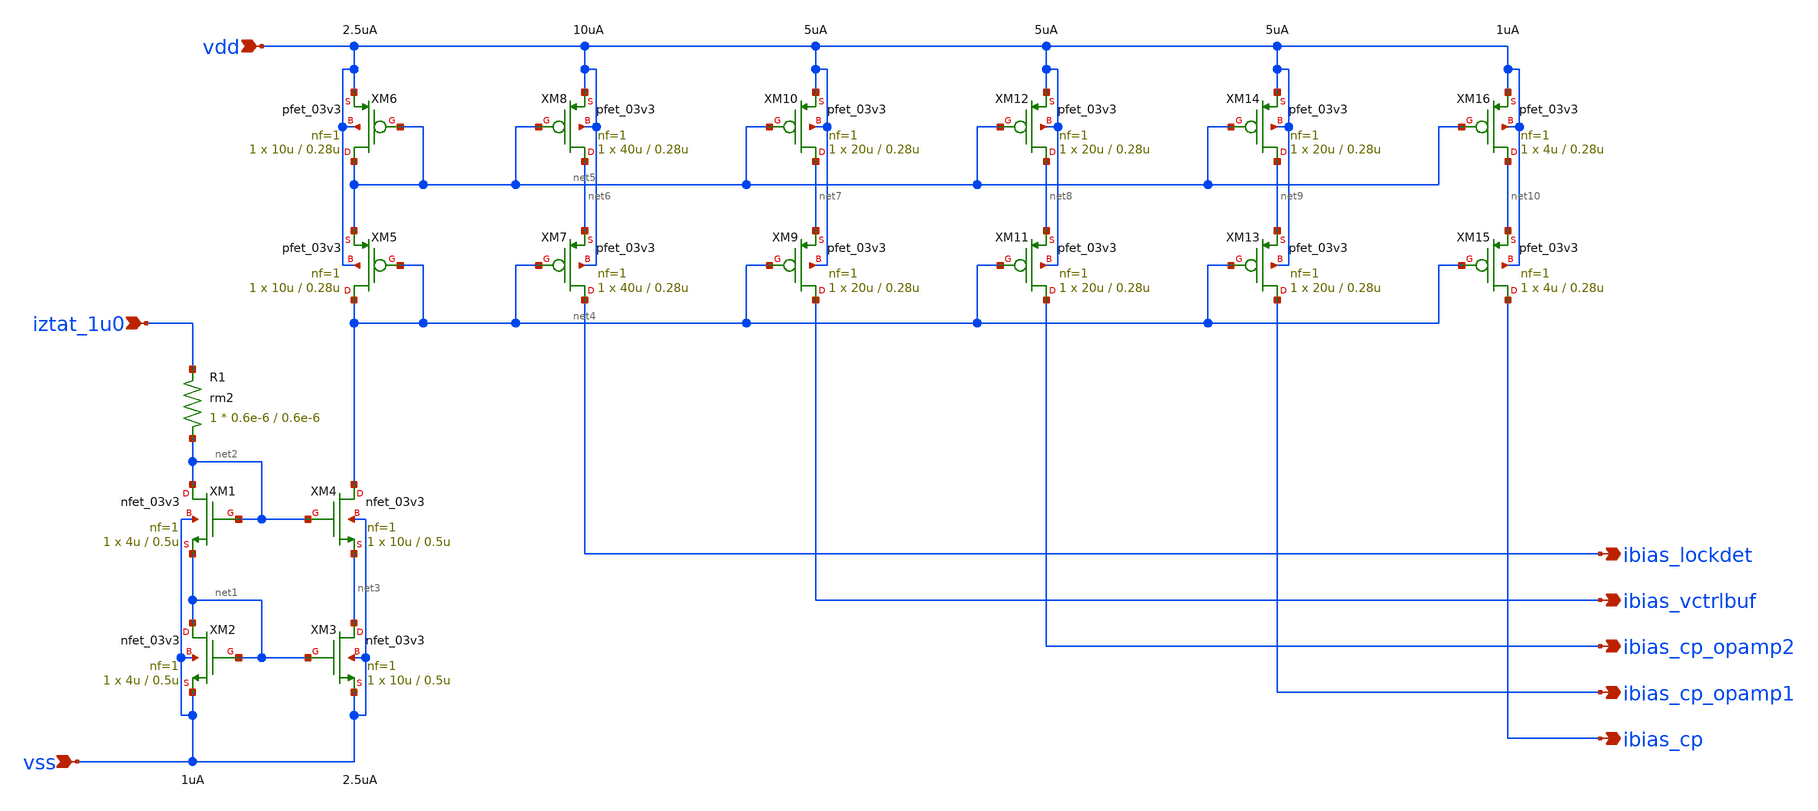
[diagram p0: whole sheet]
** sch_path: xschem/pll_ibias_generator.sch
**.subckt pll_ibias_generator iztat_1u0 vss vdd ibias_cp ibias_cp_opamp1 ibias_cp_opamp2
*+ ibias_vctrlbuf ibias_lockdet
*.ipin iztat_1u0
*.ipin vss
*.ipin vdd
*.opin ibias_cp
*.opin ibias_cp_opamp1
*.opin ibias_cp_opamp2
*.opin ibias_vctrlbuf
*.opin ibias_lockdet
XM2 net1 net1 vss vss nfet_03v3 L=0.5u W=4u nf=1 ad='int((nf+1)/2) * W/nf * 0.18u' as='int((nf+2)/2) * W/nf * 0.18u'
+ pd='2*int((nf+1)/2) * (W/nf + 0.18u)' ps='2*int((nf+2)/2) * (W/nf + 0.18u)' nrd='0.18u / W' nrs='0.18u / W'
+ sa=0 sb=0 sd=0 m=1
XM1 net2 net2 net1 vss nfet_03v3 L=0.5u W=4u nf=1 ad='int((nf+1)/2) * W/nf * 0.18u' as='int((nf+2)/2) * W/nf * 0.18u'
+ pd='2*int((nf+1)/2) * (W/nf + 0.18u)' ps='2*int((nf+2)/2) * (W/nf + 0.18u)' nrd='0.18u / W' nrs='0.18u / W'
+ sa=0 sb=0 sd=0 m=1
XR1 net2 iztat_1u0 rm2 r_width=0.6e-6 r_length=0.6e-6 m=1
XM3 net3 net1 vss vss nfet_03v3 L=0.5u W=10u nf=1 ad='int((nf+1)/2) * W/nf * 0.18u' as='int((nf+2)/2) * W/nf * 0.18u'
+ pd='2*int((nf+1)/2) * (W/nf + 0.18u)' ps='2*int((nf+2)/2) * (W/nf + 0.18u)' nrd='0.18u / W' nrs='0.18u / W'
+ sa=0 sb=0 sd=0 m=1
XM4 net4 net2 net3 vss nfet_03v3 L=0.5u W=10u nf=1 ad='int((nf+1)/2) * W/nf * 0.18u' as='int((nf+2)/2) * W/nf * 0.18u'
+ pd='2*int((nf+1)/2) * (W/nf + 0.18u)' ps='2*int((nf+2)/2) * (W/nf + 0.18u)' nrd='0.18u / W' nrs='0.18u / W'
+ sa=0 sb=0 sd=0 m=1
XM5 net4 net4 net5 vdd pfet_03v3 L=0.28u W=10u nf=1 ad='int((nf+1)/2) * W/nf * 0.18u' as='int((nf+2)/2) * W/nf * 0.18u'
+ pd='2*int((nf+1)/2) * (W/nf + 0.18u)' ps='2*int((nf+2)/2) * (W/nf + 0.18u)' nrd='0.18u / W' nrs='0.18u / W'
+ sa=0 sb=0 sd=0 m=1
XM6 net5 net5 vdd vdd pfet_03v3 L=0.28u W=10u nf=1 ad='int((nf+1)/2) * W/nf * 0.18u' as='int((nf+2)/2) * W/nf * 0.18u'
+ pd='2*int((nf+1)/2) * (W/nf + 0.18u)' ps='2*int((nf+2)/2) * (W/nf + 0.18u)' nrd='0.18u / W' nrs='0.18u / W'
+ sa=0 sb=0 sd=0 m=1
XM7 ibias_lockdet net4 net6 vdd pfet_03v3 L=0.28u W=40u nf=1 ad='int((nf+1)/2) * W/nf * 0.18u' as='int((nf+2)/2) * W/nf * 0.18u'
+ pd='2*int((nf+1)/2) * (W/nf + 0.18u)' ps='2*int((nf+2)/2) * (W/nf + 0.18u)' nrd='0.18u / W' nrs='0.18u / W'
+ sa=0 sb=0 sd=0 m=1
XM8 net6 net5 vdd vdd pfet_03v3 L=0.28u W=40u nf=1 ad='int((nf+1)/2) * W/nf * 0.18u' as='int((nf+2)/2) * W/nf * 0.18u'
+ pd='2*int((nf+1)/2) * (W/nf + 0.18u)' ps='2*int((nf+2)/2) * (W/nf + 0.18u)' nrd='0.18u / W' nrs='0.18u / W'
+ sa=0 sb=0 sd=0 m=1
XM9 ibias_vctrlbuf net4 net7 vdd pfet_03v3 L=0.28u W=20u nf=1 ad='int((nf+1)/2) * W/nf * 0.18u' as='int((nf+2)/2) * W/nf * 0.18u'
+ pd='2*int((nf+1)/2) * (W/nf + 0.18u)' ps='2*int((nf+2)/2) * (W/nf + 0.18u)' nrd='0.18u / W' nrs='0.18u / W'
+ sa=0 sb=0 sd=0 m=1
XM10 net7 net5 vdd vdd pfet_03v3 L=0.28u W=20u nf=1 ad='int((nf+1)/2) * W/nf * 0.18u' as='int((nf+2)/2) * W/nf * 0.18u'
+ pd='2*int((nf+1)/2) * (W/nf + 0.18u)' ps='2*int((nf+2)/2) * (W/nf + 0.18u)' nrd='0.18u / W' nrs='0.18u / W'
+ sa=0 sb=0 sd=0 m=1
XM11 ibias_cp_opamp2 net4 net8 vdd pfet_03v3 L=0.28u W=20u nf=1 ad='int((nf+1)/2) * W/nf * 0.18u' as='int((nf+2)/2) * W/nf * 0.18u'
+ pd='2*int((nf+1)/2) * (W/nf + 0.18u)' ps='2*int((nf+2)/2) * (W/nf + 0.18u)' nrd='0.18u / W' nrs='0.18u / W'
+ sa=0 sb=0 sd=0 m=1
XM12 net8 net5 vdd vdd pfet_03v3 L=0.28u W=20u nf=1 ad='int((nf+1)/2) * W/nf * 0.18u' as='int((nf+2)/2) * W/nf * 0.18u'
+ pd='2*int((nf+1)/2) * (W/nf + 0.18u)' ps='2*int((nf+2)/2) * (W/nf + 0.18u)' nrd='0.18u / W' nrs='0.18u / W'
+ sa=0 sb=0 sd=0 m=1
XM13 ibias_cp_opamp1 net4 net9 vdd pfet_03v3 L=0.28u W=20u nf=1 ad='int((nf+1)/2) * W/nf * 0.18u' as='int((nf+2)/2) * W/nf * 0.18u'
+ pd='2*int((nf+1)/2) * (W/nf + 0.18u)' ps='2*int((nf+2)/2) * (W/nf + 0.18u)' nrd='0.18u / W' nrs='0.18u / W'
+ sa=0 sb=0 sd=0 m=1
XM14 net9 net5 vdd vdd pfet_03v3 L=0.28u W=20u nf=1 ad='int((nf+1)/2) * W/nf * 0.18u' as='int((nf+2)/2) * W/nf * 0.18u'
+ pd='2*int((nf+1)/2) * (W/nf + 0.18u)' ps='2*int((nf+2)/2) * (W/nf + 0.18u)' nrd='0.18u / W' nrs='0.18u / W'
+ sa=0 sb=0 sd=0 m=1
XM15 ibias_cp net4 net10 vdd pfet_03v3 L=0.28u W=4u nf=1 ad='int((nf+1)/2) * W/nf * 0.18u' as='int((nf+2)/2) * W/nf * 0.18u'
+ pd='2*int((nf+1)/2) * (W/nf + 0.18u)' ps='2*int((nf+2)/2) * (W/nf + 0.18u)' nrd='0.18u / W' nrs='0.18u / W'
+ sa=0 sb=0 sd=0 m=1
XM16 net10 net5 vdd vdd pfet_03v3 L=0.28u W=4u nf=1 ad='int((nf+1)/2) * W/nf * 0.18u' as='int((nf+2)/2) * W/nf * 0.18u'
+ pd='2*int((nf+1)/2) * (W/nf + 0.18u)' ps='2*int((nf+2)/2) * (W/nf + 0.18u)' nrd='0.18u / W' nrs='0.18u / W'
+ sa=0 sb=0 sd=0 m=1
**.ends
.end
